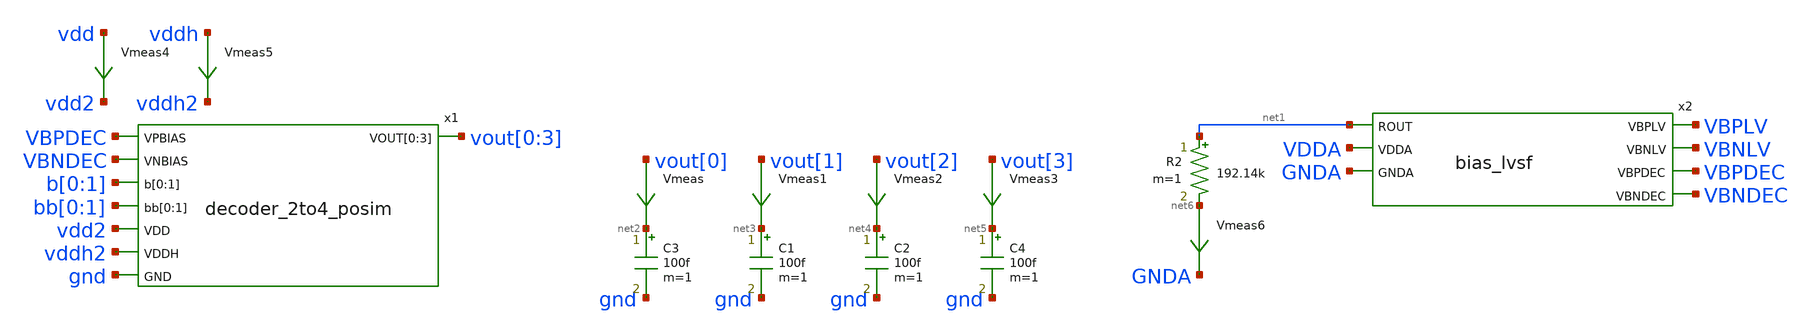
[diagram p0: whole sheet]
** sch_path: xschem/decoder_2to4-tb.sch
.lib $::SKYWATER_MODELS/sky130.lib.spice tt
.include $::SKYWATER_STDCELLS/sky130_fd_sc_hd.spice

**.subckt decoder_2to4-tb
Vmeas vout[0] net2 0
.save i(vmeas)
Vmeas1 vout[1] net3 0
.save i(vmeas1)
C3 net2 gnd 100f m=1
Vmeas2 vout[2] net4 0
.save i(vmeas2)
Vmeas3 vout[3] net5 0
.save i(vmeas3)
C1 net3 gnd 100f m=1
C2 net4 gnd 100f m=1
C4 net5 gnd 100f m=1
Vmeas4 vdd vdd2 0
.save i(vmeas4)
Vmeas5 vddh vddh2 0
.save i(vmeas5)
R2 net1 net6 192.14k m=1
Vmeas6 net6 GNDA 0
.save i(vmeas6)
x2 net1 VBPLV VBNLV VBPDEC VBNDEC VDDA GNDA bias_lvsf
x1 VBPDEC VBNDEC b[0] b[1] bb[0] bb[1] vout[0] vout[1] vout[2] vout[3] vdd2 vddh2 gnd
+ decoder_2to4_posim
**** begin user architecture code


.include $THESIS_WS/spice/decoder_2to4-tb.sp

**** end user architecture code
**.ends

* expanding   symbol:  bias_lvsf.sym # of pins=7
** sym_path: xschem/bias_lvsf.sym
** sch_path: xschem/bias_lvsf.sch
.subckt bias_lvsf ROUT VBPLV VBNLV VBPDEC VBNDEC VDDA GNDA
*.ipin ROUT
*.opin VBPLV
*.opin VBNLV
*.opin VBPDEC
*.opin VBNDEC
*.ipin VDDA
*.ipin GNDA
.param wp_iref=1.8 wn_iref=0.6 miref=2 lref=1 lr=20
XM1 n1 n1 VDDA VDDA sky130_fd_pr__pfet_g5v0d10v5 L=1 W=1.8 nf=1 ad='int((nf+1)/2) * W/nf * 0.29' as='int((nf+2)/2) * W/nf * 0.29'
+ pd='2*int((nf+1)/2) * (W/nf + 0.29)' ps='2*int((nf+2)/2) * (W/nf + 0.29)' nrd='0.29 / W' nrs='0.29 / W'
+ sa=0 sb=0 sd=0 mult=2 m=2
XM2 n2 n2 n1 VDDA sky130_fd_pr__pfet_g5v0d10v5 L=1 W=1.8 nf=1 ad='int((nf+1)/2) * W/nf * 0.29' as='int((nf+2)/2) * W/nf * 0.29'
+ pd='2*int((nf+1)/2) * (W/nf + 0.29)' ps='2*int((nf+2)/2) * (W/nf + 0.29)' nrd='0.29 / W' nrs='0.29 / W'
+ sa=0 sb=0 sd=0 mult=2 m=2
XM3 net1 ROUT n2 VDDA sky130_fd_pr__pfet_g5v0d10v5 L=20 W=1.8 nf=1 ad='int((nf+1)/2) * W/nf * 0.29' as='int((nf+2)/2) * W/nf * 0.29'
+ pd='2*int((nf+1)/2) * (W/nf + 0.29)' ps='2*int((nf+2)/2) * (W/nf + 0.29)' nrd='0.29 / W' nrs='0.29 / W'
+ sa=0 sb=0 sd=0 mult=2 m=2
XM4 ROUT ROUT net1 VDDA sky130_fd_pr__pfet_g5v0d10v5 L=20 W=1.8 nf=1 ad='int((nf+1)/2) * W/nf * 0.29'
+ as='int((nf+2)/2) * W/nf * 0.29' pd='2*int((nf+1)/2) * (W/nf + 0.29)' ps='2*int((nf+2)/2) * (W/nf + 0.29)'
+ nrd='0.29 / W' nrs='0.29 / W' sa=0 sb=0 sd=0 mult=2 m=2
XM5 net2 n1 VDDA VDDA sky130_fd_pr__pfet_g5v0d10v5 L=1 W=1.8 nf=1 ad='int((nf+1)/2) * W/nf * 0.29' as='int((nf+2)/2) * W/nf * 0.29'
+ pd='2*int((nf+1)/2) * (W/nf + 0.29)' ps='2*int((nf+2)/2) * (W/nf + 0.29)' nrd='0.29 / W' nrs='0.29 / W'
+ sa=0 sb=0 sd=0 mult=2 m=2
XM6 n3 n2 net2 VDDA sky130_fd_pr__pfet_g5v0d10v5 L=1 W=1.8 nf=1 ad='int((nf+1)/2) * W/nf * 0.29' as='int((nf+2)/2) * W/nf * 0.29'
+ pd='2*int((nf+1)/2) * (W/nf + 0.29)' ps='2*int((nf+2)/2) * (W/nf + 0.29)' nrd='0.29 / W' nrs='0.29 / W'
+ sa=0 sb=0 sd=0 mult=2 m=2
XM9 net3 n1 VDDA VDDA sky130_fd_pr__pfet_g5v0d10v5 L=1 W=1.8 nf=1 ad='int((nf+1)/2) * W/nf * 0.29' as='int((nf+2)/2) * W/nf * 0.29'
+ pd='2*int((nf+1)/2) * (W/nf + 0.29)' ps='2*int((nf+2)/2) * (W/nf + 0.29)' nrd='0.29 / W' nrs='0.29 / W'
+ sa=0 sb=0 sd=0 mult=2 m=2
XM10 VBNLV n2 net3 VDDA sky130_fd_pr__pfet_g5v0d10v5 L=1 W=1.8 nf=1 ad='int((nf+1)/2) * W/nf * 0.29'
+ as='int((nf+2)/2) * W/nf * 0.29' pd='2*int((nf+1)/2) * (W/nf + 0.29)' ps='2*int((nf+2)/2) * (W/nf + 0.29)'
+ nrd='0.29 / W' nrs='0.29 / W' sa=0 sb=0 sd=0 mult=2 m=2
XM11 net4 n1 VDDA VDDA sky130_fd_pr__pfet_g5v0d10v5 L=1 W=1.8 nf=1 ad='int((nf+1)/2) * W/nf * 0.29' as='int((nf+2)/2) * W/nf * 0.29'
+ pd='2*int((nf+1)/2) * (W/nf + 0.29)' ps='2*int((nf+2)/2) * (W/nf + 0.29)' nrd='0.29 / W' nrs='0.29 / W'
+ sa=0 sb=0 sd=0 mult=2 m=2
XM12 VBNDEC n2 net4 VDDA sky130_fd_pr__pfet_g5v0d10v5 L=1 W=1.8 nf=1 ad='int((nf+1)/2) * W/nf * 0.29'
+ as='int((nf+2)/2) * W/nf * 0.29' pd='2*int((nf+1)/2) * (W/nf + 0.29)' ps='2*int((nf+2)/2) * (W/nf + 0.29)'
+ nrd='0.29 / W' nrs='0.29 / W' sa=0 sb=0 sd=0 mult=2 m=2
XM22 net6 n1 VDDA VDDA sky130_fd_pr__pfet_g5v0d10v5 L=1 W=1.8 nf=1 ad='int((nf+1)/2) * W/nf * 0.29' as='int((nf+2)/2) * W/nf * 0.29'
+ pd='2*int((nf+1)/2) * (W/nf + 0.29)' ps='2*int((nf+2)/2) * (W/nf + 0.29)' nrd='0.29 / W' nrs='0.29 / W'
+ sa=0 sb=0 sd=0 mult=2 m=2
XM23 VBPDEC n2 net6 VDDA sky130_fd_pr__pfet_g5v0d10v5 L=1 W=1.8 nf=1 ad='int((nf+1)/2) * W/nf * 0.29'
+ as='int((nf+2)/2) * W/nf * 0.29' pd='2*int((nf+1)/2) * (W/nf + 0.29)' ps='2*int((nf+2)/2) * (W/nf + 0.29)'
+ nrd='0.29 / W' nrs='0.29 / W' sa=0 sb=0 sd=0 mult=2 m=2
XM7 n3 n3 n4 GNDA sky130_fd_pr__nfet_g5v0d10v5 L=1 W=0.6 nf=1 ad='int((nf+1)/2) * W/nf * 0.29' as='int((nf+2)/2) * W/nf * 0.29'
+ pd='2*int((nf+1)/2) * (W/nf + 0.29)' ps='2*int((nf+2)/2) * (W/nf + 0.29)' nrd='0.29 / W' nrs='0.29 / W'
+ sa=0 sb=0 sd=0 mult=2 m=2
XM8 n4 n4 GNDA GNDA sky130_fd_pr__nfet_g5v0d10v5 L=1 W=0.6 nf=1 ad='int((nf+1)/2) * W/nf * 0.29' as='int((nf+2)/2) * W/nf * 0.29'
+ pd='2*int((nf+1)/2) * (W/nf + 0.29)' ps='2*int((nf+2)/2) * (W/nf + 0.29)' nrd='0.29 / W' nrs='0.29 / W'
+ sa=0 sb=0 sd=0 mult=2 m=2
XM13 VBPLV n3 net5 GNDA sky130_fd_pr__nfet_g5v0d10v5 L=1 W=0.6 nf=1 ad='int((nf+1)/2) * W/nf * 0.29'
+ as='int((nf+2)/2) * W/nf * 0.29' pd='2*int((nf+1)/2) * (W/nf + 0.29)' ps='2*int((nf+2)/2) * (W/nf + 0.29)'
+ nrd='0.29 / W' nrs='0.29 / W' sa=0 sb=0 sd=0 mult=2 m=2
XM15 net5 n4 GNDA GNDA sky130_fd_pr__nfet_g5v0d10v5 L=1 W=0.6 nf=1 ad='int((nf+1)/2) * W/nf * 0.29' as='int((nf+2)/2) * W/nf * 0.29'
+ pd='2*int((nf+1)/2) * (W/nf + 0.29)' ps='2*int((nf+2)/2) * (W/nf + 0.29)' nrd='0.29 / W' nrs='0.29 / W'
+ sa=0 sb=0 sd=0 mult=2 m=2
XM19 VBNLV VBNLV n6 GNDA sky130_fd_pr__nfet_g5v0d10v5 L=1 W=0.6 nf=1 ad='int((nf+1)/2) * W/nf * 0.29'
+ as='int((nf+2)/2) * W/nf * 0.29' pd='2*int((nf+1)/2) * (W/nf + 0.29)' ps='2*int((nf+2)/2) * (W/nf + 0.29)'
+ nrd='0.29 / W' nrs='0.29 / W' sa=0 sb=0 sd=0 mult=2 m=2
XM20 VBNDEC VBNDEC n7 GNDA sky130_fd_pr__nfet_g5v0d10v5 L=1 W=0.6 nf=1 ad='int((nf+1)/2) * W/nf * 0.29'
+ as='int((nf+2)/2) * W/nf * 0.29' pd='2*int((nf+1)/2) * (W/nf + 0.29)' ps='2*int((nf+2)/2) * (W/nf + 0.29)'
+ nrd='0.29 / W' nrs='0.29 / W' sa=0 sb=0 sd=0 mult=2 m=2
XM25 VBPDEC VBPDEC n14 GNDA sky130_fd_pr__nfet_g5v0d10v5 L=1 W=0.6 nf=1 ad='int((nf+1)/2) * W/nf * 0.29'
+ as='int((nf+2)/2) * W/nf * 0.29' pd='2*int((nf+1)/2) * (W/nf + 0.29)' ps='2*int((nf+2)/2) * (W/nf + 0.29)'
+ nrd='0.29 / W' nrs='0.29 / W' sa=0 sb=0 sd=0 mult=2 m=2
XM14 n6 VBNLV GNDA GNDA sky130_fd_pr__nfet_g5v0d10v5 L=5.3 W=0.6 nf=1 ad='int((nf+1)/2) * W/nf * 0.29'
+ as='int((nf+2)/2) * W/nf * 0.29' pd='2*int((nf+1)/2) * (W/nf + 0.29)' ps='2*int((nf+2)/2) * (W/nf + 0.29)'
+ nrd='0.29 / W' nrs='0.29 / W' sa=0 sb=0 sd=0 mult=1 m=1
XM16 n7 VBNDEC GNDA GNDA sky130_fd_pr__nfet_g5v0d10v5 L=9.7 W=0.61 nf=1 ad='int((nf+1)/2) * W/nf * 0.29'
+ as='int((nf+2)/2) * W/nf * 0.29' pd='2*int((nf+1)/2) * (W/nf + 0.29)' ps='2*int((nf+2)/2) * (W/nf + 0.29)'
+ nrd='0.29 / W' nrs='0.29 / W' sa=0 sb=0 sd=0 mult=1 m=1
XM27 n14 n14 GNDA GNDA sky130_fd_pr__nfet_g5v0d10v5 L=12 W=0.64 nf=1 ad='int((nf+1)/2) * W/nf * 0.29'
+ as='int((nf+2)/2) * W/nf * 0.29' pd='2*int((nf+1)/2) * (W/nf + 0.29)' ps='2*int((nf+2)/2) * (W/nf + 0.29)'
+ nrd='0.29 / W' nrs='0.29 / W' sa=0 sb=0 sd=0 mult=1 m=1
XM18 VBPLV VBPLV n10 VDDA sky130_fd_pr__pfet_g5v0d10v5 L=1 W=1.8 nf=1 ad='int((nf+1)/2) * W/nf * 0.29'
+ as='int((nf+2)/2) * W/nf * 0.29' pd='2*int((nf+1)/2) * (W/nf + 0.29)' ps='2*int((nf+2)/2) * (W/nf + 0.29)'
+ nrd='0.29 / W' nrs='0.29 / W' sa=0 sb=0 sd=0 mult=2 m=2
XM17 n10 VBPLV VDDA VDDA sky130_fd_pr__pfet_g5v0d10v5 L=9.2 W=1 nf=1 ad='int((nf+1)/2) * W/nf * 0.29'
+ as='int((nf+2)/2) * W/nf * 0.29' pd='2*int((nf+1)/2) * (W/nf + 0.29)' ps='2*int((nf+2)/2) * (W/nf + 0.29)'
+ nrd='0.29 / W' nrs='0.29 / W' sa=0 sb=0 sd=0 mult=1 m=1
XM28 VDDA VDDA VDDA VDDA sky130_fd_pr__pfet_g5v0d10v5 L=20 W=1.8 nf=1 ad='int((nf+1)/2) * W/nf * 0.29'
+ as='int((nf+2)/2) * W/nf * 0.29' pd='2*int((nf+1)/2) * (W/nf + 0.29)' ps='2*int((nf+2)/2) * (W/nf + 0.29)'
+ nrd='0.29 / W' nrs='0.29 / W' sa=0 sb=0 sd=0 mult=2 m=2
XM29 VDDA VDDA VDDA VDDA sky130_fd_pr__pfet_g5v0d10v5 L=20 W=1.8 nf=1 ad='int((nf+1)/2) * W/nf * 0.29'
+ as='int((nf+2)/2) * W/nf * 0.29' pd='2*int((nf+1)/2) * (W/nf + 0.29)' ps='2*int((nf+2)/2) * (W/nf + 0.29)'
+ nrd='0.29 / W' nrs='0.29 / W' sa=0 sb=0 sd=0 mult=2 m=2
.ends

.end
